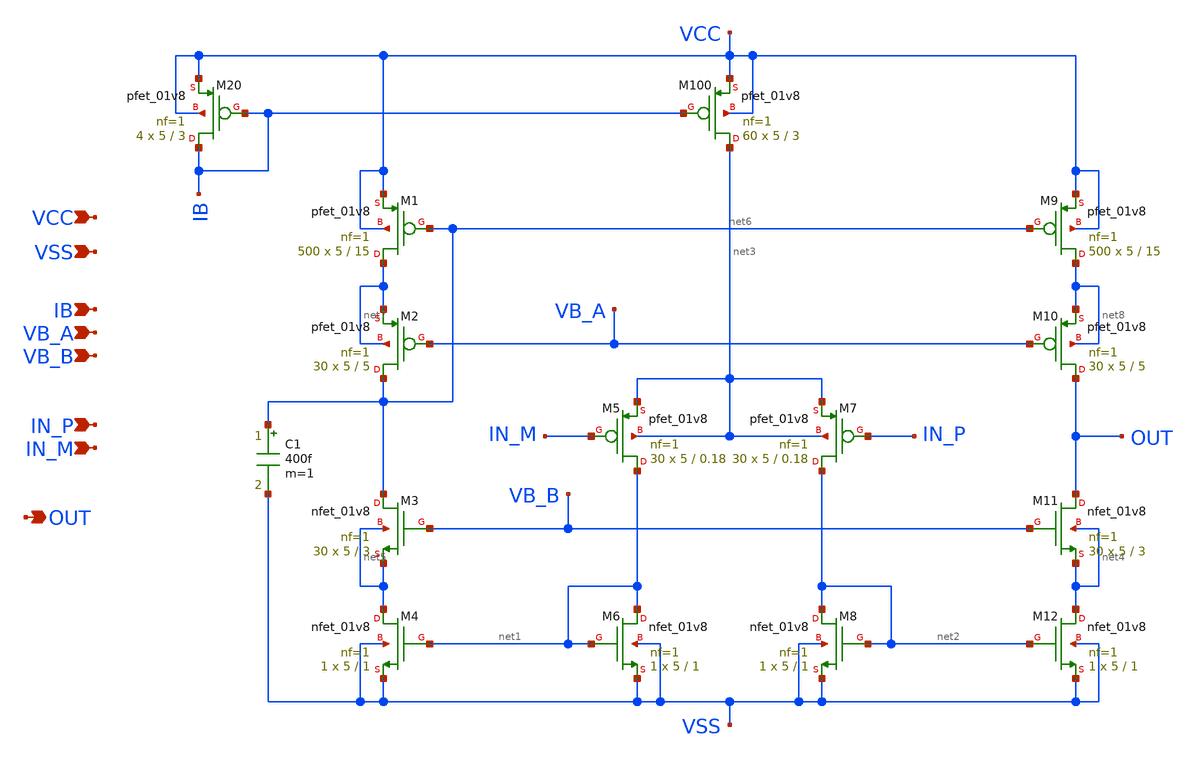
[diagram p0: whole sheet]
** sch_path: opamp_cascode.sch
**.subckt opamp_cascode IN_P IN_M VCC VSS OUT VB_A VB_B IB
*.ipin IN_P
*.ipin IN_M
*.ipin VCC
*.ipin VSS
*.opin OUT
*.ipin VB_A
*.ipin VB_B
*.ipin IB
XM9 net8 net6 VCC VCC sky130_fd_pr__pfet_01v8 L=15 W=5 nf=1 ad='int((nf+1)/2) * W/nf * 0.29' as='int((nf+2)/2) * W/nf * 0.29'
+ pd='2*int((nf+1)/2) * (W/nf + 0.29)' ps='2*int((nf+2)/2) * (W/nf + 0.29)' nrd='0.29 / W' nrs='0.29 / W'
+ sa=0 sb=0 sd=0 mult=500 m=500
XM1 net7 net6 VCC VCC sky130_fd_pr__pfet_01v8 L=15 W=5 nf=1 ad='int((nf+1)/2) * W/nf * 0.29' as='int((nf+2)/2) * W/nf * 0.29'
+ pd='2*int((nf+1)/2) * (W/nf + 0.29)' ps='2*int((nf+2)/2) * (W/nf + 0.29)' nrd='0.29 / W' nrs='0.29 / W'
+ sa=0 sb=0 sd=0 mult=500 m=500
XM100 net3 IB VCC VCC sky130_fd_pr__pfet_01v8 L=3 W=5 nf=1 ad='int((nf+1)/2) * W/nf * 0.29' as='int((nf+2)/2) * W/nf * 0.29'
+ pd='2*int((nf+1)/2) * (W/nf + 0.29)' ps='2*int((nf+2)/2) * (W/nf + 0.29)' nrd='0.29 / W' nrs='0.29 / W'
+ sa=0 sb=0 sd=0 mult=60 m=60
XM20 IB IB VCC VCC sky130_fd_pr__pfet_01v8 L=3 W=5 nf=1 ad='int((nf+1)/2) * W/nf * 0.29' as='int((nf+2)/2) * W/nf * 0.29'
+ pd='2*int((nf+1)/2) * (W/nf + 0.29)' ps='2*int((nf+2)/2) * (W/nf + 0.29)' nrd='0.29 / W' nrs='0.29 / W'
+ sa=0 sb=0 sd=0 mult=4 m=4
XM10 OUT VB_A net8 net8 sky130_fd_pr__pfet_01v8 L=5 W=5 nf=1 ad='int((nf+1)/2) * W/nf * 0.29' as='int((nf+2)/2) * W/nf * 0.29'
+ pd='2*int((nf+1)/2) * (W/nf + 0.29)' ps='2*int((nf+2)/2) * (W/nf + 0.29)' nrd='0.29 / W' nrs='0.29 / W'
+ sa=0 sb=0 sd=0 mult=30 m=30
XM2 net6 VB_A net7 net7 sky130_fd_pr__pfet_01v8 L=5 W=5 nf=1 ad='int((nf+1)/2) * W/nf * 0.29' as='int((nf+2)/2) * W/nf * 0.29'
+ pd='2*int((nf+1)/2) * (W/nf + 0.29)' ps='2*int((nf+2)/2) * (W/nf + 0.29)' nrd='0.29 / W' nrs='0.29 / W'
+ sa=0 sb=0 sd=0 mult=30 m=30
XM5 net1 IN_M net3 net3 sky130_fd_pr__pfet_01v8 L=0.18 W=5 nf=1 ad='int((nf+1)/2) * W/nf * 0.29' as='int((nf+2)/2) * W/nf * 0.29'
+ pd='2*int((nf+1)/2) * (W/nf + 0.29)' ps='2*int((nf+2)/2) * (W/nf + 0.29)' nrd='0.29 / W' nrs='0.29 / W'
+ sa=0 sb=0 sd=0 mult=30 m=30
XM7 net2 IN_P net3 net3 sky130_fd_pr__pfet_01v8 L=0.18 W=5 nf=1 ad='int((nf+1)/2) * W/nf * 0.29' as='int((nf+2)/2) * W/nf * 0.29'
+ pd='2*int((nf+1)/2) * (W/nf + 0.29)' ps='2*int((nf+2)/2) * (W/nf + 0.29)' nrd='0.29 / W' nrs='0.29 / W'
+ sa=0 sb=0 sd=0 mult=30 m=30
XM6 net1 net1 VSS VSS sky130_fd_pr__nfet_01v8 L=1 W=5 nf=1 ad='int((nf+1)/2) * W/nf * 0.29' as='int((nf+2)/2) * W/nf * 0.29'
+ pd='2*int((nf+1)/2) * (W/nf + 0.29)' ps='2*int((nf+2)/2) * (W/nf + 0.29)' nrd='0.29 / W' nrs='0.29 / W'
+ sa=0 sb=0 sd=0 mult=1 m=1
XM8 net2 net2 VSS VSS sky130_fd_pr__nfet_01v8 L=1 W=5 nf=1 ad='int((nf+1)/2) * W/nf * 0.29' as='int((nf+2)/2) * W/nf * 0.29'
+ pd='2*int((nf+1)/2) * (W/nf + 0.29)' ps='2*int((nf+2)/2) * (W/nf + 0.29)' nrd='0.29 / W' nrs='0.29 / W'
+ sa=0 sb=0 sd=0 mult=1 m=1
XM12 net4 net2 VSS VSS sky130_fd_pr__nfet_01v8 L=1 W=5 nf=1 ad='int((nf+1)/2) * W/nf * 0.29' as='int((nf+2)/2) * W/nf * 0.29'
+ pd='2*int((nf+1)/2) * (W/nf + 0.29)' ps='2*int((nf+2)/2) * (W/nf + 0.29)' nrd='0.29 / W' nrs='0.29 / W'
+ sa=0 sb=0 sd=0 mult=1 m=1
XM4 net5 net1 VSS VSS sky130_fd_pr__nfet_01v8 L=1 W=5 nf=1 ad='int((nf+1)/2) * W/nf * 0.29' as='int((nf+2)/2) * W/nf * 0.29'
+ pd='2*int((nf+1)/2) * (W/nf + 0.29)' ps='2*int((nf+2)/2) * (W/nf + 0.29)' nrd='0.29 / W' nrs='0.29 / W'
+ sa=0 sb=0 sd=0 mult=1 m=1
XM11 OUT VB_B net4 net4 sky130_fd_pr__nfet_01v8 L=3 W=5 nf=1 ad='int((nf+1)/2) * W/nf * 0.29' as='int((nf+2)/2) * W/nf * 0.29'
+ pd='2*int((nf+1)/2) * (W/nf + 0.29)' ps='2*int((nf+2)/2) * (W/nf + 0.29)' nrd='0.29 / W' nrs='0.29 / W'
+ sa=0 sb=0 sd=0 mult=30 m=30
XM3 net6 VB_B net5 net5 sky130_fd_pr__nfet_01v8 L=3 W=5 nf=1 ad='int((nf+1)/2) * W/nf * 0.29' as='int((nf+2)/2) * W/nf * 0.29'
+ pd='2*int((nf+1)/2) * (W/nf + 0.29)' ps='2*int((nf+2)/2) * (W/nf + 0.29)' nrd='0.29 / W' nrs='0.29 / W'
+ sa=0 sb=0 sd=0 mult=30 m=30
C1 net6 VSS 400f m=1
**.ends
.end
